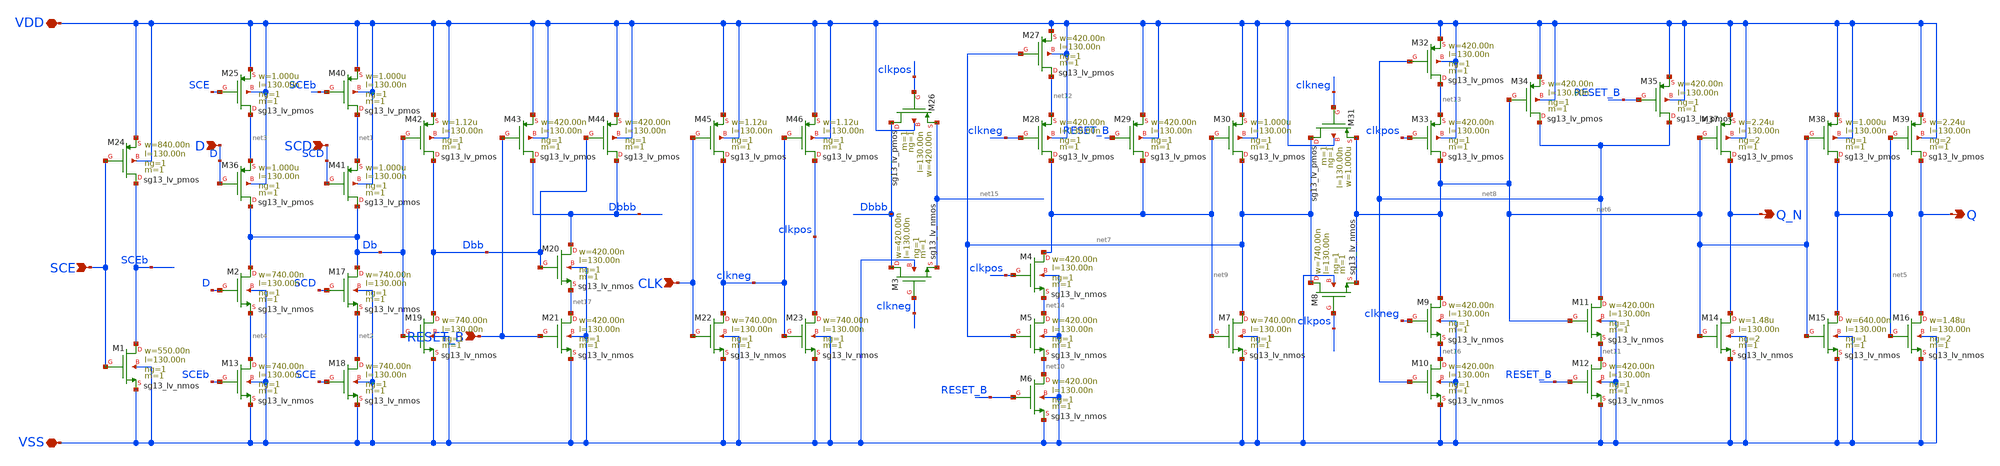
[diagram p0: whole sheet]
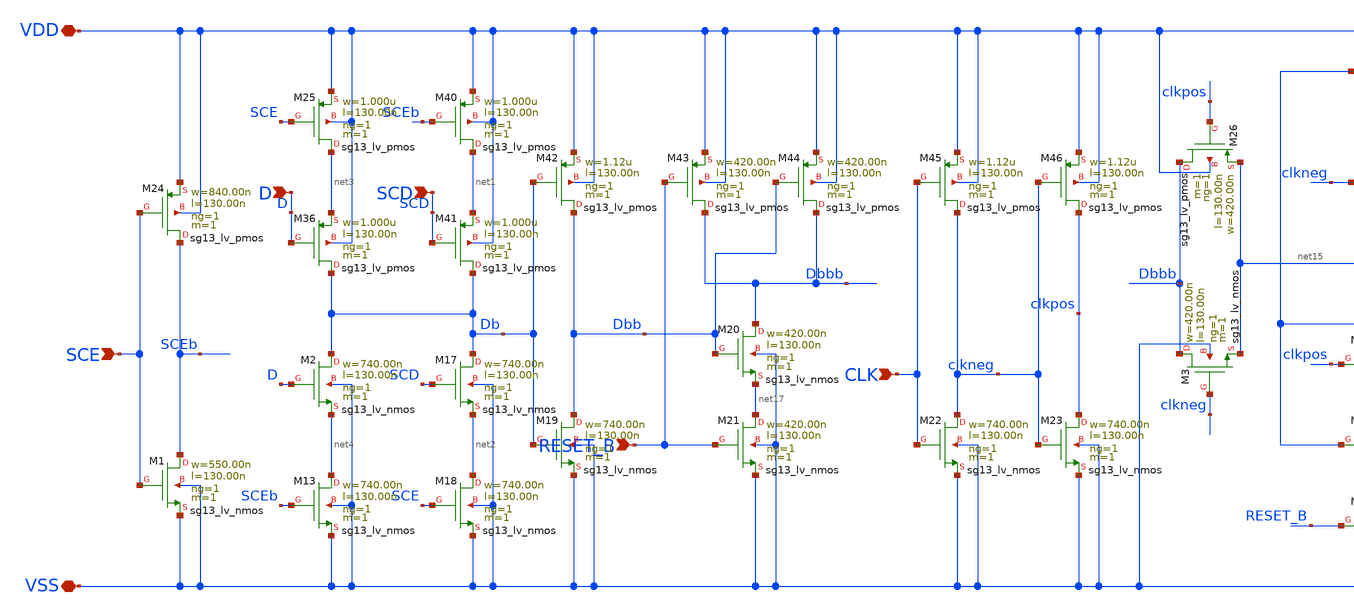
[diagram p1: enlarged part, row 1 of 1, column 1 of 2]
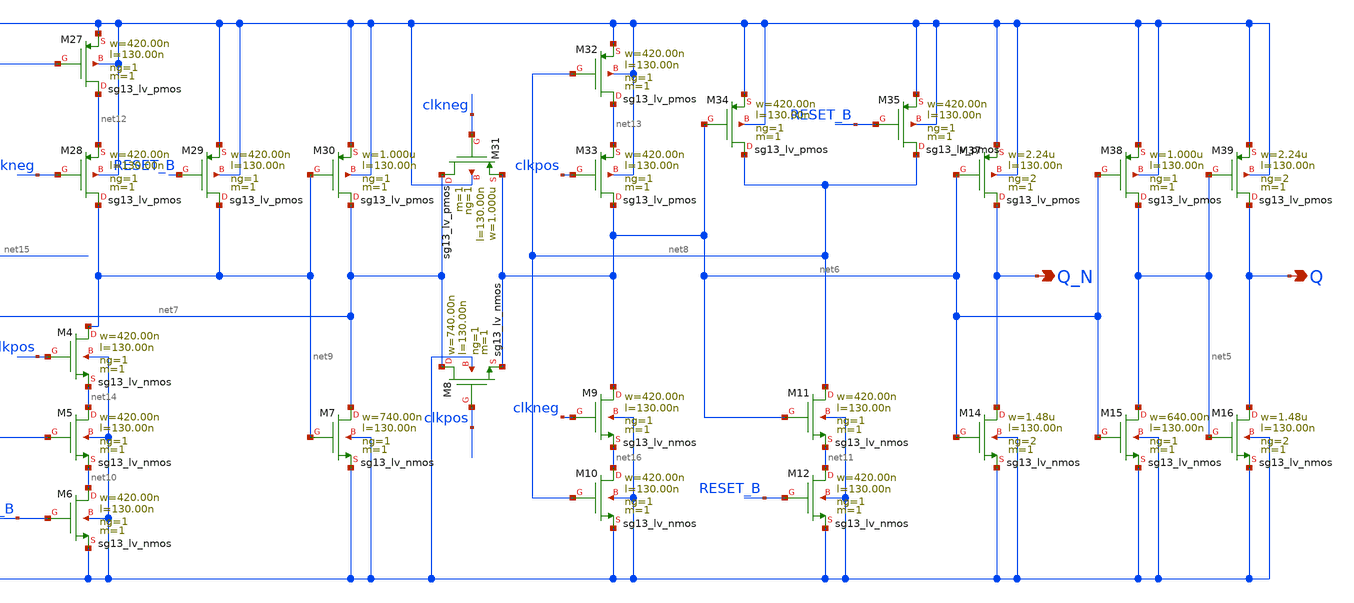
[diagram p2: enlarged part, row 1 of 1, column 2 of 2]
** sch_path: ihp-sg13g2/libs.tech/xschem/sg13g2_stdcells/sg13g2_sdfrbp_2.sch
* Copyright 2023 IHP PDK Authors
* Licensed under the Apache License, Version 2.0 (the "License");
* you may not use this file except in compliance with the License.
* You may obtain a copy of the License at
* https://www.apache.org/licenses/LICENSE-2.0
* Unless required by applicable law or agreed to in writing, software
* distributed under the License is distributed on an "AS IS" BASIS,
* WITHOUT WARRANTIES OR CONDITIONS OF ANY KIND, either express or implied.
* See the License for the specific language governing permissions and
* limitations under the License.
**.subckt sg13g2_sdfrbp_2 Q Q_N CLK D RESET_B SCD SCE VDD VSS
*.opin Q
*.opin Q_N
*.ipin CLK
*.ipin D
*.ipin RESET_B
*.ipin SCD
*.ipin SCE
*.iopin VDD
*.iopin VSS
XM1 SCEb SCE VSS VSS sg13_lv_nmos w=550.00n l=130.00n ng=1 m=1 mm_ok=1
XM2 Db D net4 VSS sg13_lv_nmos w=740.00n l=130.00n ng=1 m=1 mm_ok=1
XM3 Dbbb clkneg net15 VSS sg13_lv_nmos w=420.00n l=130.00n ng=1 m=1 mm_ok=1
XM4 net9 clkpos net14 VSS sg13_lv_nmos w=420.00n l=130.00n ng=1 m=1 mm_ok=1
XM5 net14 net7 net10 VSS sg13_lv_nmos w=420.00n l=130.00n ng=1 m=1 mm_ok=1
XM6 net10 RESET_B VSS VSS sg13_lv_nmos w=420.00n l=130.00n ng=1 m=1 mm_ok=1
XM7 net7 net9 VSS VSS sg13_lv_nmos w=740.00n l=130.00n ng=1 m=1 mm_ok=1
XM8 net7 clkpos net6 VSS sg13_lv_nmos w=740.00n l=130.00n ng=1 m=1 mm_ok=1
XM9 net6 clkneg net16 VSS sg13_lv_nmos w=420.00n l=130.00n ng=1 m=1 mm_ok=1
XM10 net16 net8 VSS VSS sg13_lv_nmos w=420.00n l=130.00n ng=1 m=1 mm_ok=1
XM11 net8 net6 net11 VSS sg13_lv_nmos w=420.00n l=130.00n ng=1 m=1 mm_ok=1
XM12 net11 RESET_B VSS VSS sg13_lv_nmos w=420.00n l=130.00n ng=1 m=1 mm_ok=1
XM13 net4 SCEb VSS VSS sg13_lv_nmos w=740.00n l=130.00n ng=1 m=1 mm_ok=1
XM14 Q_N net6 VSS VSS sg13_lv_nmos w=1.48u l=130.00n ng=2 m=1 mm_ok=1
XM15 net5 net6 VSS VSS sg13_lv_nmos w=640.00n l=130.00n ng=1 m=1 mm_ok=1
XM16 Q net5 VSS VSS sg13_lv_nmos w=1.48u l=130.00n ng=2 m=1 mm_ok=1
XM17 Db SCD net2 VSS sg13_lv_nmos w=740.00n l=130.00n ng=1 m=1 mm_ok=1
XM18 net2 SCE VSS VSS sg13_lv_nmos w=740.00n l=130.00n ng=1 m=1 mm_ok=1
XM19 Dbb Db VSS VSS sg13_lv_nmos w=740.00n l=130.00n ng=1 m=1 mm_ok=1
XM20 Dbbb Dbb net17 VSS sg13_lv_nmos w=420.00n l=130.00n ng=1 m=1 mm_ok=1
XM21 net17 RESET_B VSS VSS sg13_lv_nmos w=420.00n l=130.00n ng=1 m=1 mm_ok=1
XM22 clkneg CLK VSS VSS sg13_lv_nmos w=740.00n l=130.00n ng=1 m=1 mm_ok=1
XM23 clkpos clkneg VSS VSS sg13_lv_nmos w=740.00n l=130.00n ng=1 m=1 mm_ok=1
XM24 SCEb SCE VDD VDD sg13_lv_pmos w=840.00n l=130.00n ng=1 m=1 mm_ok=1
XM25 net3 SCE VDD VDD sg13_lv_pmos w=1.000u l=130.00n ng=1 m=1 mm_ok=1
XM26 Dbbb clkpos net15 VDD sg13_lv_pmos w=420.00n l=130.00n ng=1 m=1 mm_ok=1
XM27 net12 net7 VDD VDD sg13_lv_pmos w=420.00n l=130.00n ng=1 m=1 mm_ok=1
XM28 net9 clkneg net12 VDD sg13_lv_pmos w=420.00n l=130.00n ng=1 m=1 mm_ok=1
XM29 net9 RESET_B VDD VDD sg13_lv_pmos w=420.00n l=130.00n ng=1 m=1 mm_ok=1
XM30 net7 net9 VDD VDD sg13_lv_pmos w=1.000u l=130.00n ng=1 m=1 mm_ok=1
XM31 net7 clkneg net6 VDD sg13_lv_pmos w=1.000u l=130.00n ng=1 m=1 mm_ok=1
XM32 net13 net8 VDD VDD sg13_lv_pmos w=420.00n l=130.00n ng=1 m=1 mm_ok=1
XM33 net6 clkpos net13 VDD sg13_lv_pmos w=420.00n l=130.00n ng=1 m=1 mm_ok=1
XM34 net8 net6 VDD VDD sg13_lv_pmos w=420.00n l=130.00n ng=1 m=1 mm_ok=1
XM35 net8 RESET_B VDD VDD sg13_lv_pmos w=420.00n l=130.00n ng=1 m=1 mm_ok=1
XM36 Db D net3 VDD sg13_lv_pmos w=1.000u l=130.00n ng=1 m=1 mm_ok=1
XM37 Q_N net6 VDD VDD sg13_lv_pmos w=2.24u l=130.00n ng=2 m=1 mm_ok=1
XM38 net5 net6 VDD VDD sg13_lv_pmos w=1.000u l=130.00n ng=1 m=1 mm_ok=1
XM39 Q net5 VDD VDD sg13_lv_pmos w=2.24u l=130.00n ng=2 m=1 mm_ok=1
XM40 net1 SCEb VDD VDD sg13_lv_pmos w=1.000u l=130.00n ng=1 m=1 mm_ok=1
XM41 Db SCD net1 VDD sg13_lv_pmos w=1.000u l=130.00n ng=1 m=1 mm_ok=1
XM42 Dbb Db VDD VDD sg13_lv_pmos w=1.12u l=130.00n ng=1 m=1 mm_ok=1
XM43 Dbbb RESET_B VDD VDD sg13_lv_pmos w=420.00n l=130.00n ng=1 m=1 mm_ok=1
XM44 Dbbb Dbb VDD VDD sg13_lv_pmos w=420.00n l=130.00n ng=1 m=1 mm_ok=1
XM45 clkneg CLK VDD VDD sg13_lv_pmos w=1.12u l=130.00n ng=1 m=1 mm_ok=1
XM46 clkpos clkneg VDD VDD sg13_lv_pmos w=1.12u l=130.00n ng=1 m=1 mm_ok=1
**.ends
.end
